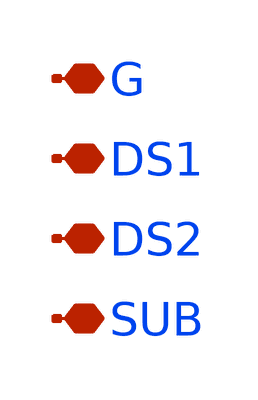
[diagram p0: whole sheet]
** sch_path: xschem/rf_nfet_6xaM02_extracted.sch
**.subckt rf_nfet_6xaM02_extracted G DS1 DS2 SUB
*.iopin G
*.iopin DS1
*.iopin DS2
*.iopin SUB
**** begin user architecture code


* Extraction of 6xaM02 (12 finger) Transistors
* wt=60um, L=0.15um
.subckt NFET_extract_1 SD1 G2 SD2 SUB

* .subckt sky130_fd_pr__rf_nfet_01v8_aM02W5p00L0p15 DRAIN GATE SOURCE SUBSTRATE
*  X0 DRAIN GATE SOURCE SUBSTRATE sky130_fd_pr__nfet_01v8 ad=1.414e+12p pd=1.066e+07u as=2.828e+12p
*+ ps=2.132e+07u w=5.05e+06u l=150000u
*  X1 SOURCE GATE DRAIN SUBSTRATE sky130_fd_pr__nfet_01v8 ad=0p pd=0u as=0p ps=0u w=5.05e+06u
*+ l=150000u
*  C0 SOURCE DRAIN 3.73fF
*  C1 SOURCE SUBSTRATE 2.58fF
* .ends

X0 SD1 G2 SD2 SUB sky130_fd_pr__nfet_01v8 ad=0p pd=0u as=0p ps=0u w=5.05e+06u l=150000u
X1 SD1 G2 SD2 SUB sky130_fd_pr__nfet_01v8 ad=0p pd=0u as=0p ps=0u w=5.05e+06u l=150000u
X2 SD2 G2 SD1 SUB sky130_fd_pr__nfet_01v8 ad=0p pd=0u as=0p ps=0u w=5.05e+06u l=150000u
X3 SD2 G2 SD1 SUB sky130_fd_pr__nfet_01v8 ad=0p pd=0u as=0p ps=0u w=5.05e+06u l=150000u
X4 SD1 G2 SD2 SUB sky130_fd_pr__nfet_01v8 ad=0p pd=0u as=0p ps=0u w=5.05e+06u l=150000u
X5 SD1 G2 SD2 SUB sky130_fd_pr__nfet_01v8 ad=0p pd=0u as=0p ps=0u w=5.05e+06u l=150000u
X6 SD2 G2 SD1 SUB sky130_fd_pr__nfet_01v8 ad=0p pd=0u as=0p ps=0u w=5.05e+06u l=150000u
X7 SD2 G2 SD1 SUB sky130_fd_pr__nfet_01v8 ad=0p pd=0u as=0p ps=0u w=5.05e+06u l=150000u
X8 SD1 G2 SD2 SUB sky130_fd_pr__nfet_01v8 ad=0p pd=0u as=0p ps=0u w=5.05e+06u l=150000u
X9 SD1 G2 SD2 SUB sky130_fd_pr__nfet_01v8 ad=0p pd=0u as=0p ps=0u w=5.05e+06u l=150000u
X10 SD2 G2 SD1 SUB sky130_fd_pr__nfet_01v8 ad=0p pd=0u as=0p ps=0u w=5.05e+06u l=150000u
X11 SD2 G2 SD1 SUB sky130_fd_pr__nfet_01v8 ad=0p pd=0u as=0p ps=0u w=5.05e+06u l=150000u
C0 SD2 G2 3.50fF
C1 SUB SD1 3.01fF
C2 G2 SD1 4.50fF
C3 G2 SUB 2.28fF
C4 SD2 SD1 30.48fF
C5 G2 SUB 3.11fF
C6 SD1 SUB 6.76fF

* C0 B G 2.85fF
* C1 S D 22.23fF
* C2 G D 5.77fF
* C3 S G 7.53fF
* Xnfet_3x_2_0/sky130_fd_pr__rf_nfet_01v8_aM02W5p00L0p15_0 D G S B
*+ sky130_fd_pr__rf_nfet_01v8_aM02W5p00L0p15
* Xnfet_3x_2_0/sky130_fd_pr__rf_nfet_01v8_aM02W5p00L0p15_1 D G S B
*+ sky130_fd_pr__rf_nfet_01v8_aM02W5p00L0p15
* Xnfet_3x_2_0/sky130_fd_pr__rf_nfet_01v8_aM02W5p00L0p15_2 D G S B
*+ sky130_fd_pr__rf_nfet_01v8_aM02W5p00L0p15
* Xnfet_3x_2_1/sky130_fd_pr__rf_nfet_01v8_aM02W5p00L0p15_0 D G S B
*+ sky130_fd_pr__rf_nfet_01v8_aM02W5p00L0p15
* Xnfet_3x_2_1/sky130_fd_pr__rf_nfet_01v8_aM02W5p00L0p15_1 D G S B
*+ sky130_fd_pr__rf_nfet_01v8_aM02W5p00L0p15
* Xnfet_3x_2_1/sky130_fd_pr__rf_nfet_01v8_aM02W5p00L0p15_2 D G S B
*+ sky130_fd_pr__rf_nfet_01v8_aM02W5p00L0p15
* C4 S B 13.70fF
* C5 G B 3.35fF

.ends

XM0 DS1 G DS2 SUB NFET_extract_1


**** end user architecture code
**.ends
.end
